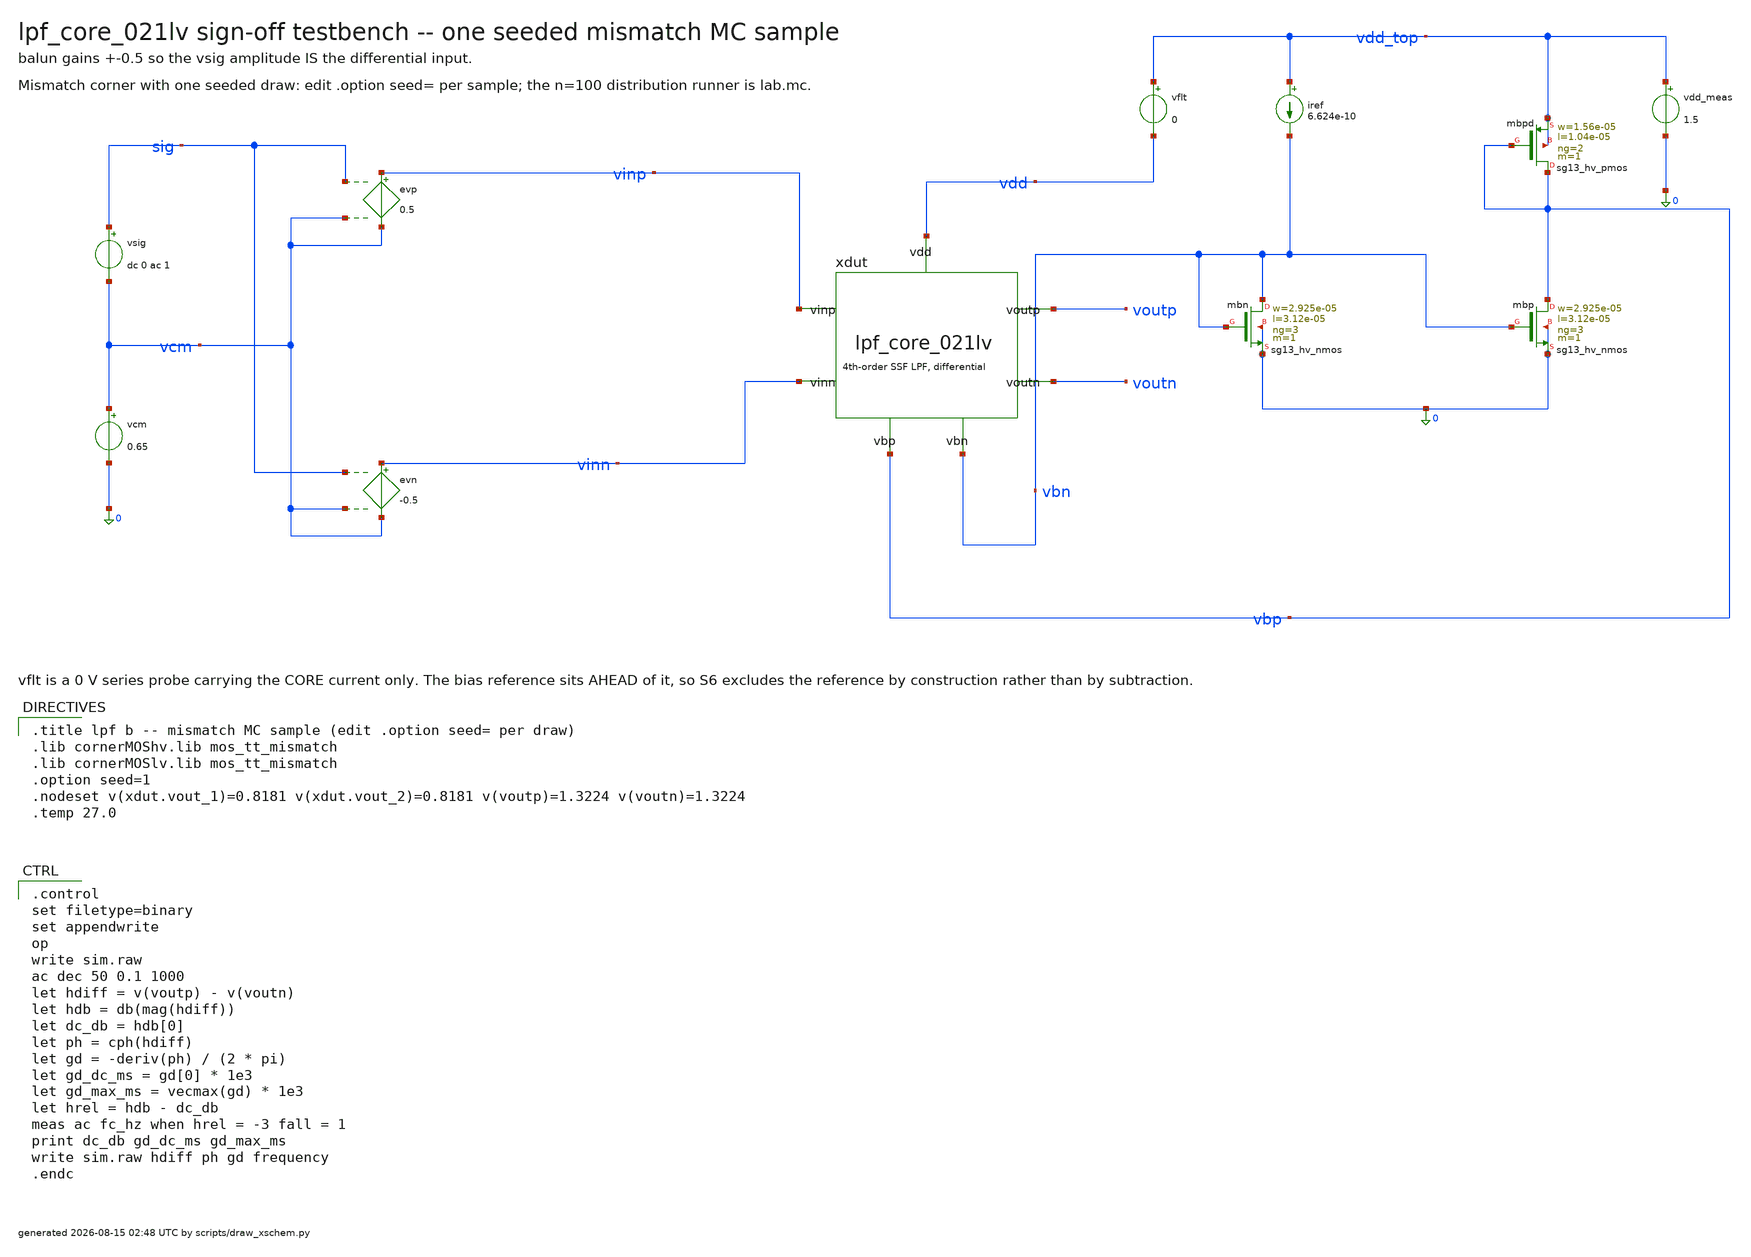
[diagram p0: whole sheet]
** sch_path: signoff/pre-pvt/schematic/lpf_tb_021lv_mc.sch
**.subckt lpf_tb_021lv_mc
vsig sig vcm dc 0 ac 1
vcm vcm 0 0.65
evp vinp vcm sig vcm 0.5
evn vinn vcm sig vcm -0.5
xdut vinp vinn voutp voutn vbn vbp vdd lpf_core_021lv
vflt vdd_top vdd 0
vdd_meas vdd_top 0 1.5
iref vdd_top vbn 6.624e-10
Xmbn vbn vbn 0 0 sg13_hv_nmos w=2.925e-05 l=3.12e-05 ng=3 m=1 mm_ok=1
Xmbp vbp vbn 0 0 sg13_hv_nmos w=2.925e-05 l=3.12e-05 ng=3 m=1 mm_ok=1
Xmbpd vbp vbp vdd_top vdd_top sg13_hv_pmos w=1.56e-05 l=1.04e-05 ng=2 m=1 mm_ok=1
**** begin user architecture code

.title lpf b -- mismatch MC sample (edit .option seed= per draw)
.lib cornerMOShv.lib mos_tt_mismatch
.lib cornerMOSlv.lib mos_tt_mismatch
.option seed=1
.nodeset v(xdut.vout_1)=0.8181 v(xdut.vout_2)=0.8181 v(voutp)=1.3224 v(voutn)=1.3224
.temp 27.0


.control
set filetype=binary
set appendwrite
op
write sim.raw
ac dec 50 0.1 1000
let hdiff = v(voutp) - v(voutn)
let hdb = db(mag(hdiff))
let dc_db = hdb[0]
let ph = cph(hdiff)
let gd = -deriv(ph) / (2 * pi)
let gd_dc_ms = gd[0] * 1e3
let gd_max_ms = vecmax(gd) * 1e3
let hrel = hdb - dc_db
meas ac fc_hz when hrel = -3 fall = 1
print dc_db gd_dc_ms gd_max_ms
write sim.raw hdiff ph gd frequency
.endc

**** end user architecture code
**.ends

* expanding   symbol:  lpf_core_021lv.sym # of pins=7
** sym_path: signoff/schematic/lpf_core_021lv.sym
** sch_path: signoff/schematic/lpf_core_021lv.sch
.subckt lpf_core_021lv vinp vinn voutp voutn vbn vbp vdd
*.ipin vinp
*.ipin vinn
*.opin voutp
*.opin voutn
*.ipin vdd
*.ipin vbn
*.ipin vbp
Xm2 net2 vinp vout_1 vout_1 sg13_lv_pmos w=1.56e-05 l=1.04e-05 ng=2 m=1 mm_ok=1
Xm5 net3 vinn vout_2 vout_2 sg13_lv_pmos w=1.56e-05 l=1.04e-05 ng=2 m=1 mm_ok=1
Xm4 vout_1 net2 0 0 sg13_hv_nmos w=7.8e-06 l=5.2e-06 ng=1 m=1 mm_ok=1
Xm8 vout_2 net3 0 0 sg13_hv_nmos w=7.8e-06 l=5.2e-06 ng=1 m=1 mm_ok=1
Xm9 net2 vbn 0 0 sg13_hv_nmos w=2.925e-05 l=3.12e-05 ng=3 m=1 mm_ok=1
Xm10 net3 vbn 0 0 sg13_hv_nmos w=2.925e-05 l=3.12e-05 ng=3 m=1 mm_ok=1
Xmst vout_1 vbn net4 net4 sg13_hv_pmos w=1.62e-06 l=1.092e-05 ng=1 m=1 mm_ok=1
Xmstn vout_2 vbn net1 net1 sg13_hv_pmos w=1.62e-06 l=1.092e-05 ng=1 m=1 mm_ok=1
Xm0 net4 vout_1 voutp voutp sg13_hv_pmos w=1.56e-05 l=1.04e-05 ng=2 m=1 mm_ok=1
Xm1 net1 vout_2 voutn voutn sg13_hv_pmos w=1.56e-05 l=1.04e-05 ng=2 m=1 mm_ok=1
Xm14 voutp net4 vdd vdd sg13_hv_pmos w=8.085e-06 l=1.56e-05 ng=1 m=1 mm_ok=1
Xm15 voutn net1 vdd vdd sg13_hv_pmos w=8.085e-06 l=1.56e-05 ng=1 m=1 mm_ok=1
c13 net2 vout_1 6.58174e-12 m=1
c17 net3 vout_2 6.58174e-12 m=1
c19 vout_2 vout_1 2.65642e-11 m=1
c1 voutp net4 5.18878e-11 m=1
c10 voutn net1 5.18878e-11 m=1
c12 voutn voutp 2.04984e-11 m=1
.ends

.end
